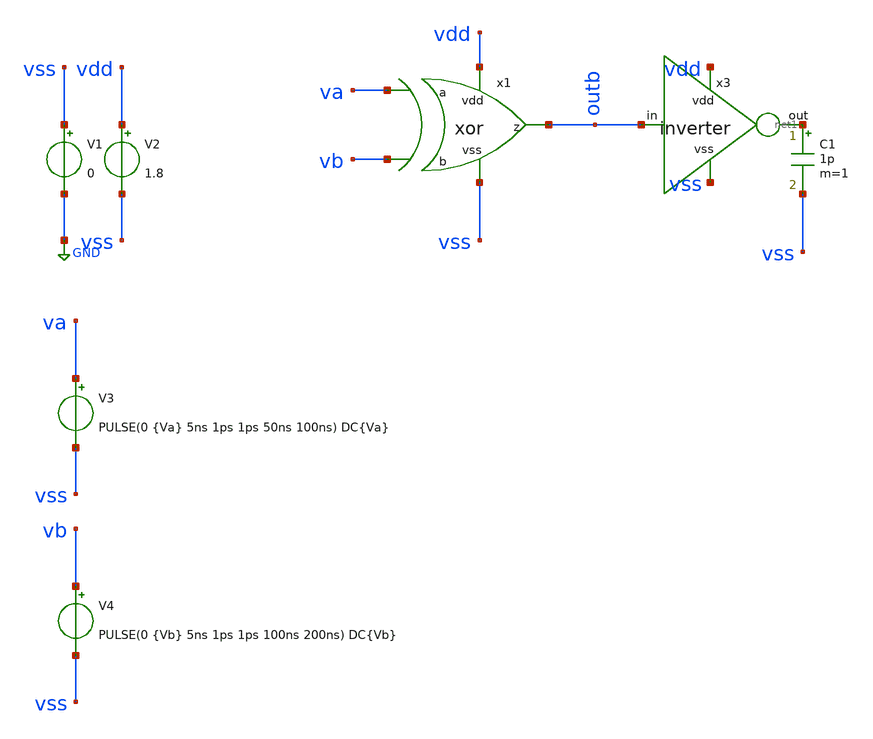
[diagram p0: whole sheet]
** sch_path: track_vlsi/ledesma/sch/tb_xor.sch
**.subckt tb_xor
V1 vss GND 0
V2 vdd vss 1.8
V3 va vss PULSE(0 {Va} 5ns 1ps 1ps 50ns 100ns) DC{Va}
V4 vb vss PULSE(0 {Vb} 5ns 1ps 1ps 100ns 200ns) DC{Vb}
x3 vdd net1 outb vss inverter
C1 net1 vss 1p m=1
x1 vdd va vb outb vss xor
**** begin user architecture code



* Parametros del circuito
.param Va=1.8
.param Vb=1.8
.options TEMP = 27.0

* Include
.lib /home/eamta/skywater/skywater-pdk/libraries/sky130_fd_pr_ngspice/latest/models/corners/sky130.lib TT

*simulation
.control
  tran 1n 200ns
  setplot tran1
  plot v(outb) v(Va)+1.8 V(Vb)+3.6
  write tb_and_tran.raw

  reset
  dc V3 0 1.8 0.01
  setplot dc1
  plot v(outb) v(Va)
  write tb_inverter_dc.ra

.endc
.end


**** end user architecture code
**.ends
.GLOBAL GND
.end
